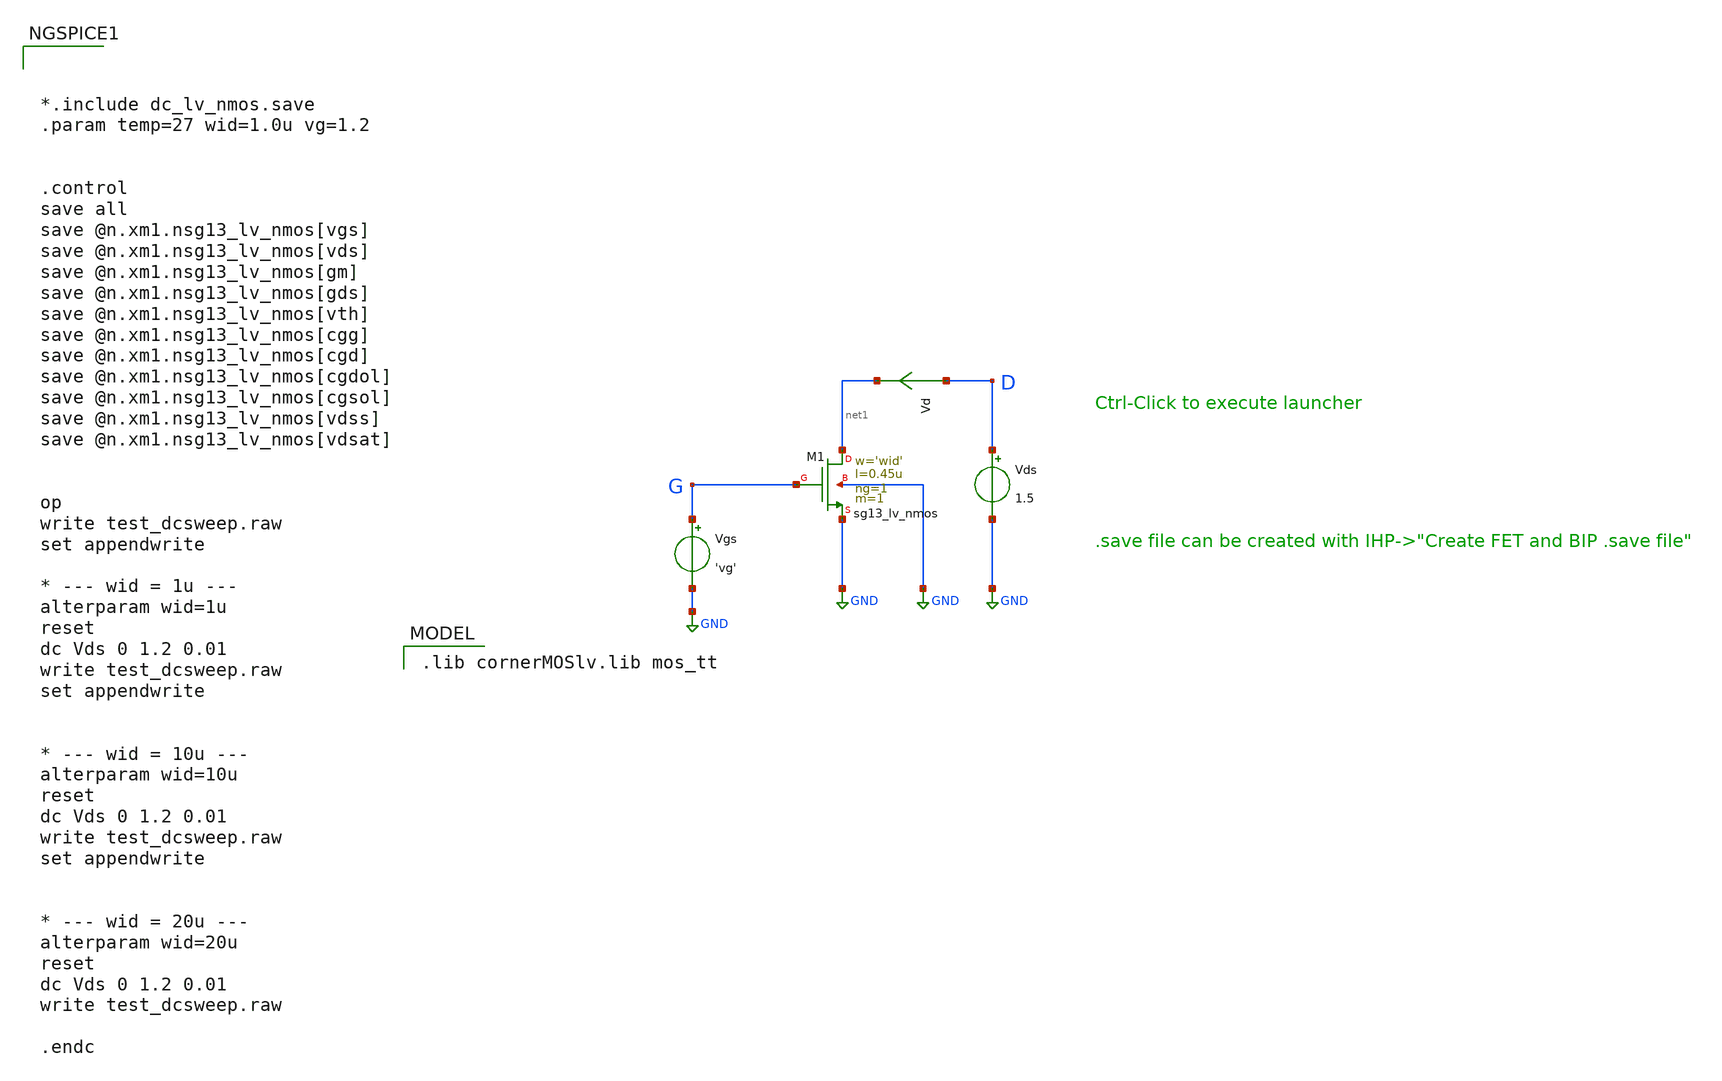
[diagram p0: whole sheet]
** sch_path: xschem/test_dcsweep.sch
* Copyright 2023 IHP PDK Authors
**.subckt test_dcsweep
Vgs G GND 'vg'
Vds D GND 1.5
Vd D net1 0
.save i(vd)
XM1 net1 G GND GND sg13_lv_nmos w='wid' l=0.45u ng=1 m=1 mm_ok=1
**** begin user architecture code
 .lib cornerMOSlv.lib mos_tt




*.include dc_lv_nmos.save
.param temp=27 wid=1.0u vg=1.2


.control
save all
save @n.xm1.nsg13_lv_nmos[vgs]
save @n.xm1.nsg13_lv_nmos[vds]
save @n.xm1.nsg13_lv_nmos[gm]
save @n.xm1.nsg13_lv_nmos[gds]
save @n.xm1.nsg13_lv_nmos[vth]
save @n.xm1.nsg13_lv_nmos[cgg]
save @n.xm1.nsg13_lv_nmos[cgd]
save @n.xm1.nsg13_lv_nmos[cgdol]
save @n.xm1.nsg13_lv_nmos[cgsol]
save @n.xm1.nsg13_lv_nmos[vdss]
save @n.xm1.nsg13_lv_nmos[vdsat]


op
write test_dcsweep.raw
set appendwrite

* --- wid = 1u ---
alterparam wid=1u
reset
dc Vds 0 1.2 0.01
write test_dcsweep.raw
set appendwrite


* --- wid = 10u ---
alterparam wid=10u
reset
dc Vds 0 1.2 0.01
write test_dcsweep.raw
set appendwrite


* --- wid = 20u ---
alterparam wid=20u
reset
dc Vds 0 1.2 0.01
write test_dcsweep.raw

.endc



**** end user architecture code
**.ends
.GLOBAL GND
.end
